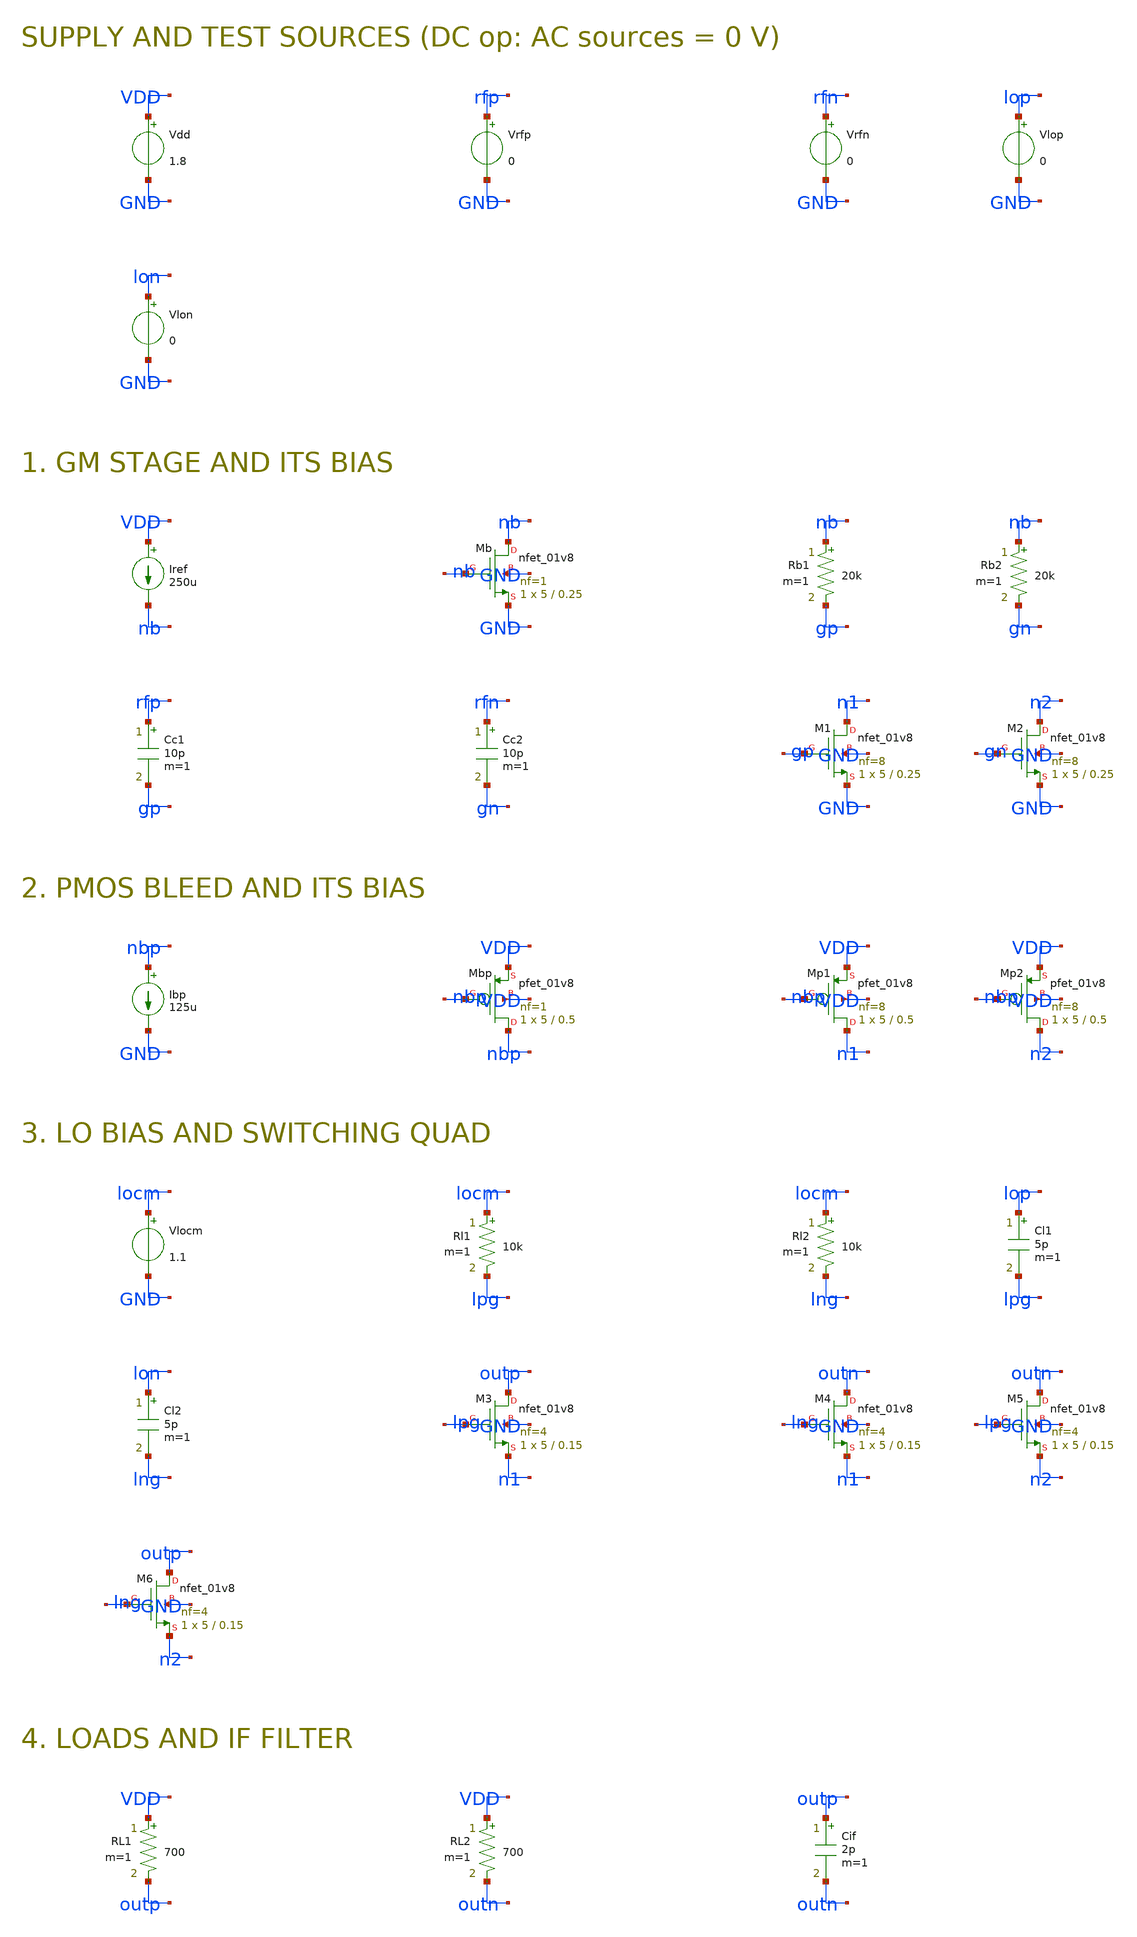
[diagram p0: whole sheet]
** sch_path: 09-sky130-gilbert-mixer-rfic/schematics/gilbert_dc.sch
**.subckt gilbert_dc
Vdd VDD GND 1.8
Vrfp rfp GND 0
Vrfn rfn GND 0
Vlop lop GND 0
Vlon lon GND 0
Iref VDD nb 250u
XMb nb nb GND GND sky130_fd_pr__nfet_01v8 L=0.25 W=5 nf=1 ad='int((nf+1)/2) * W/nf * 0.29' as='int((nf+2)/2) * W/nf * 0.29'
+ pd='2*int((nf+1)/2) * (W/nf + 0.29)' ps='2*int((nf+2)/2) * (W/nf + 0.29)' nrd='0.29 / W' nrs='0.29 / W'
+ sa=0 sb=0 sd=0 mult=1 m=1
Rb1 nb gp 20k m=1
Rb2 nb gn 20k m=1
Cc1 rfp gp 10p m=1
Cc2 rfn gn 10p m=1
XM1 n1 gp GND GND sky130_fd_pr__nfet_01v8 L=0.25 W=5 nf=8 ad='int((nf+1)/2) * W/nf * 0.29' as='int((nf+2)/2) * W/nf * 0.29'
+ pd='2*int((nf+1)/2) * (W/nf + 0.29)' ps='2*int((nf+2)/2) * (W/nf + 0.29)' nrd='0.29 / W' nrs='0.29 / W'
+ sa=0 sb=0 sd=0 mult=1 m=1
XM2 n2 gn GND GND sky130_fd_pr__nfet_01v8 L=0.25 W=5 nf=8 ad='int((nf+1)/2) * W/nf * 0.29' as='int((nf+2)/2) * W/nf * 0.29'
+ pd='2*int((nf+1)/2) * (W/nf + 0.29)' ps='2*int((nf+2)/2) * (W/nf + 0.29)' nrd='0.29 / W' nrs='0.29 / W'
+ sa=0 sb=0 sd=0 mult=1 m=1
Ibp nbp GND 125u
XMbp nbp nbp VDD VDD sky130_fd_pr__pfet_01v8 L=0.5 W=5 nf=1 ad='int((nf+1)/2) * W/nf * 0.29' as='int((nf+2)/2) * W/nf * 0.29'
+ pd='2*int((nf+1)/2) * (W/nf + 0.29)' ps='2*int((nf+2)/2) * (W/nf + 0.29)' nrd='0.29 / W' nrs='0.29 / W'
+ sa=0 sb=0 sd=0 mult=1 m=1
XMp1 n1 nbp VDD VDD sky130_fd_pr__pfet_01v8 L=0.5 W=5 nf=8 ad='int((nf+1)/2) * W/nf * 0.29' as='int((nf+2)/2) * W/nf * 0.29'
+ pd='2*int((nf+1)/2) * (W/nf + 0.29)' ps='2*int((nf+2)/2) * (W/nf + 0.29)' nrd='0.29 / W' nrs='0.29 / W'
+ sa=0 sb=0 sd=0 mult=1 m=1
XMp2 n2 nbp VDD VDD sky130_fd_pr__pfet_01v8 L=0.5 W=5 nf=8 ad='int((nf+1)/2) * W/nf * 0.29' as='int((nf+2)/2) * W/nf * 0.29'
+ pd='2*int((nf+1)/2) * (W/nf + 0.29)' ps='2*int((nf+2)/2) * (W/nf + 0.29)' nrd='0.29 / W' nrs='0.29 / W'
+ sa=0 sb=0 sd=0 mult=1 m=1
Vlocm locm GND 1.1
Rl1 locm lpg 10k m=1
Rl2 locm lng 10k m=1
Cl1 lop lpg 5p m=1
Cl2 lon lng 5p m=1
XM3 outp lpg n1 GND sky130_fd_pr__nfet_01v8 L=0.15 W=5 nf=4 ad='int((nf+1)/2) * W/nf * 0.29' as='int((nf+2)/2) * W/nf * 0.29'
+ pd='2*int((nf+1)/2) * (W/nf + 0.29)' ps='2*int((nf+2)/2) * (W/nf + 0.29)' nrd='0.29 / W' nrs='0.29 / W'
+ sa=0 sb=0 sd=0 mult=1 m=1
XM4 outn lng n1 GND sky130_fd_pr__nfet_01v8 L=0.15 W=5 nf=4 ad='int((nf+1)/2) * W/nf * 0.29' as='int((nf+2)/2) * W/nf * 0.29'
+ pd='2*int((nf+1)/2) * (W/nf + 0.29)' ps='2*int((nf+2)/2) * (W/nf + 0.29)' nrd='0.29 / W' nrs='0.29 / W'
+ sa=0 sb=0 sd=0 mult=1 m=1
XM5 outn lpg n2 GND sky130_fd_pr__nfet_01v8 L=0.15 W=5 nf=4 ad='int((nf+1)/2) * W/nf * 0.29' as='int((nf+2)/2) * W/nf * 0.29'
+ pd='2*int((nf+1)/2) * (W/nf + 0.29)' ps='2*int((nf+2)/2) * (W/nf + 0.29)' nrd='0.29 / W' nrs='0.29 / W'
+ sa=0 sb=0 sd=0 mult=1 m=1
XM6 outp lng n2 GND sky130_fd_pr__nfet_01v8 L=0.15 W=5 nf=4 ad='int((nf+1)/2) * W/nf * 0.29' as='int((nf+2)/2) * W/nf * 0.29'
+ pd='2*int((nf+1)/2) * (W/nf + 0.29)' ps='2*int((nf+2)/2) * (W/nf + 0.29)' nrd='0.29 / W' nrs='0.29 / W'
+ sa=0 sb=0 sd=0 mult=1 m=1
RL1 VDD outp 700 m=1
RL2 VDD outn 700 m=1
Cif outp outn 2p m=1
**** begin user architecture code

.lib $::SKYWATER_MODELS/sky130.lib.spice tt
.control
op
print v(nb) v(nbp) v(gp) v(n1) v(n2) v(outp) v(outn) v(lpg)
print -i(Vdd)
let il1=(1.8-v(outp))/700
let il2=(1.8-v(outn))/700
print il1 il2
.endc

**** end user architecture code
**.ends
.end
